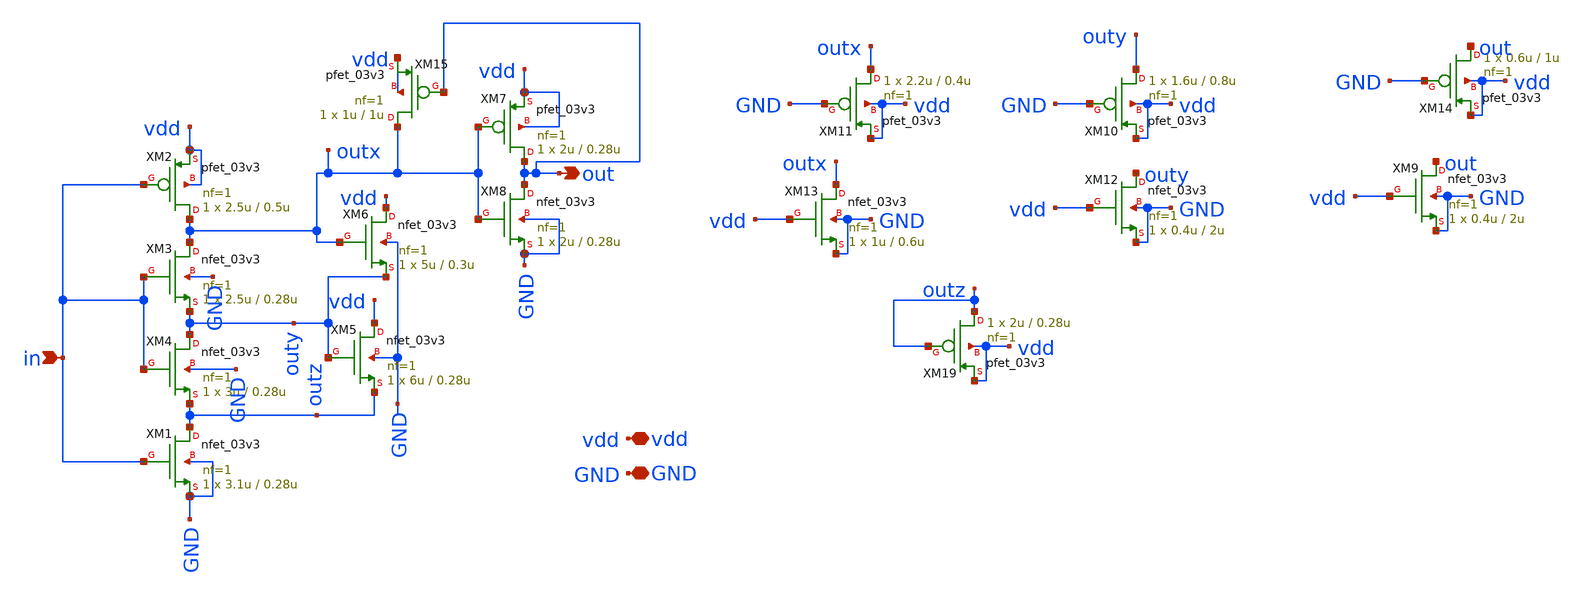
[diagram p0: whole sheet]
** sch_path: designs/libs/core_schmitt_trigger/schmitt_trigger.sch
**.subckt schmitt_trigger in out vdd GND
*.ipin in
*.opin out
*.iopin vdd
*.iopin GND
XM2 outx in vdd vdd pfet_03v3 L=0.5u W=2.5u nf=1 ad='int((nf+1)/2) * W/nf * 0.18u' as='int((nf+2)/2) * W/nf * 0.18u'
+ pd='2*int((nf+1)/2) * (W/nf + 0.18u)' ps='2*int((nf+2)/2) * (W/nf + 0.18u)' nrd='0.18u / W' nrs='0.18u / W'
+ sa=0 sb=0 sd=0 m=1
XM1 outz in GND GND nfet_03v3 L=0.28u W=3.1u nf=1 ad='int((nf+1)/2) * W/nf * 0.18u' as='int((nf+2)/2) * W/nf * 0.18u'
+ pd='2*int((nf+1)/2) * (W/nf + 0.18u)' ps='2*int((nf+2)/2) * (W/nf + 0.18u)' nrd='0.18u / W' nrs='0.18u / W'
+ sa=0 sb=0 sd=0 m=1
XM4 outy in outz GND nfet_03v3 L=0.28u W=3u nf=1 ad='int((nf+1)/2) * W/nf * 0.18u' as='int((nf+2)/2) * W/nf * 0.18u'
+ pd='2*int((nf+1)/2) * (W/nf + 0.18u)' ps='2*int((nf+2)/2) * (W/nf + 0.18u)' nrd='0.18u / W' nrs='0.18u / W'
+ sa=0 sb=0 sd=0 m=1
XM3 outx in outy GND nfet_03v3 L=0.28u W=2.5u nf=1 ad='int((nf+1)/2) * W/nf * 0.18u' as='int((nf+2)/2) * W/nf * 0.18u'
+ pd='2*int((nf+1)/2) * (W/nf + 0.18u)' ps='2*int((nf+2)/2) * (W/nf + 0.18u)' nrd='0.18u / W' nrs='0.18u / W'
+ sa=0 sb=0 sd=0 m=1
XM5 vdd outy outz GND nfet_03v3 L=0.28u W=6u nf=1 ad='int((nf+1)/2) * W/nf * 0.18u' as='int((nf+2)/2) * W/nf * 0.18u'
+ pd='2*int((nf+1)/2) * (W/nf + 0.18u)' ps='2*int((nf+2)/2) * (W/nf + 0.18u)' nrd='0.18u / W' nrs='0.18u / W'
+ sa=0 sb=0 sd=0 m=1
XM6 vdd outx outy GND nfet_03v3 L=0.3u W=5u nf=1 ad='int((nf+1)/2) * W/nf * 0.18u' as='int((nf+2)/2) * W/nf * 0.18u'
+ pd='2*int((nf+1)/2) * (W/nf + 0.18u)' ps='2*int((nf+2)/2) * (W/nf + 0.18u)' nrd='0.18u / W' nrs='0.18u / W'
+ sa=0 sb=0 sd=0 m=1
XM8 out outx GND GND nfet_03v3 L=0.28u W=2u nf=1 ad='int((nf+1)/2) * W/nf * 0.18u' as='int((nf+2)/2) * W/nf * 0.18u'
+ pd='2*int((nf+1)/2) * (W/nf + 0.18u)' ps='2*int((nf+2)/2) * (W/nf + 0.18u)' nrd='0.18u / W' nrs='0.18u / W'
+ sa=0 sb=0 sd=0 m=1
XM7 out outx vdd vdd pfet_03v3 L=0.28u W=2u nf=1 ad='int((nf+1)/2) * W/nf * 0.18u' as='int((nf+2)/2) * W/nf * 0.18u'
+ pd='2*int((nf+1)/2) * (W/nf + 0.18u)' ps='2*int((nf+2)/2) * (W/nf + 0.18u)' nrd='0.18u / W' nrs='0.18u / W'
+ sa=0 sb=0 sd=0 m=1
XM9 out vdd GND GND nfet_03v3 L=2u W=0.4u nf=1 ad='int((nf+1)/2) * W/nf * 0.18u' as='int((nf+2)/2) * W/nf * 0.18u'
+ pd='2*int((nf+1)/2) * (W/nf + 0.18u)' ps='2*int((nf+2)/2) * (W/nf + 0.18u)' nrd='0.18u / W' nrs='0.18u / W'
+ sa=0 sb=0 sd=0 m=1
XM14 out GND vdd vdd pfet_03v3 L=1u W=0.6u nf=1 ad='int((nf+1)/2) * W/nf * 0.18u' as='int((nf+2)/2) * W/nf * 0.18u'
+ pd='2*int((nf+1)/2) * (W/nf + 0.18u)' ps='2*int((nf+2)/2) * (W/nf + 0.18u)' nrd='0.18u / W' nrs='0.18u / W'
+ sa=0 sb=0 sd=0 m=1
XM10 outy GND vdd vdd pfet_03v3 L=0.8u W=1.6u nf=1 ad='int((nf+1)/2) * W/nf * 0.18u' as='int((nf+2)/2) * W/nf * 0.18u'
+ pd='2*int((nf+1)/2) * (W/nf + 0.18u)' ps='2*int((nf+2)/2) * (W/nf + 0.18u)' nrd='0.18u / W' nrs='0.18u / W'
+ sa=0 sb=0 sd=0 m=1
XM11 outx GND vdd vdd pfet_03v3 L=0.4u W=2.2u nf=1 ad='int((nf+1)/2) * W/nf * 0.18u' as='int((nf+2)/2) * W/nf * 0.18u'
+ pd='2*int((nf+1)/2) * (W/nf + 0.18u)' ps='2*int((nf+2)/2) * (W/nf + 0.18u)' nrd='0.18u / W' nrs='0.18u / W'
+ sa=0 sb=0 sd=0 m=1
XM12 outy vdd GND GND nfet_03v3 L=2u W=0.4u nf=1 ad='int((nf+1)/2) * W/nf * 0.18u' as='int((nf+2)/2) * W/nf * 0.18u'
+ pd='2*int((nf+1)/2) * (W/nf + 0.18u)' ps='2*int((nf+2)/2) * (W/nf + 0.18u)' nrd='0.18u / W' nrs='0.18u / W'
+ sa=0 sb=0 sd=0 m=1
XM13 outx vdd GND GND nfet_03v3 L=0.6u W=1u nf=1 ad='int((nf+1)/2) * W/nf * 0.18u' as='int((nf+2)/2) * W/nf * 0.18u'
+ pd='2*int((nf+1)/2) * (W/nf + 0.18u)' ps='2*int((nf+2)/2) * (W/nf + 0.18u)' nrd='0.18u / W' nrs='0.18u / W'
+ sa=0 sb=0 sd=0 m=1
XM19 outz outz vdd vdd pfet_03v3 L=0.28u W=2u nf=1 ad='int((nf+1)/2) * W/nf * 0.18u' as='int((nf+2)/2) * W/nf * 0.18u'
+ pd='2*int((nf+1)/2) * (W/nf + 0.18u)' ps='2*int((nf+2)/2) * (W/nf + 0.18u)' nrd='0.18u / W' nrs='0.18u / W'
+ sa=0 sb=0 sd=0 m=1
XM15 outx out vdd vdd pfet_03v3 L=1u W=1u nf=1 ad='int((nf+1)/2) * W/nf * 0.18u' as='int((nf+2)/2) * W/nf * 0.18u'
+ pd='2*int((nf+1)/2) * (W/nf + 0.18u)' ps='2*int((nf+2)/2) * (W/nf + 0.18u)' nrd='0.18u / W' nrs='0.18u / W'
+ sa=0 sb=0 sd=0 m=1
**.ends
.end
